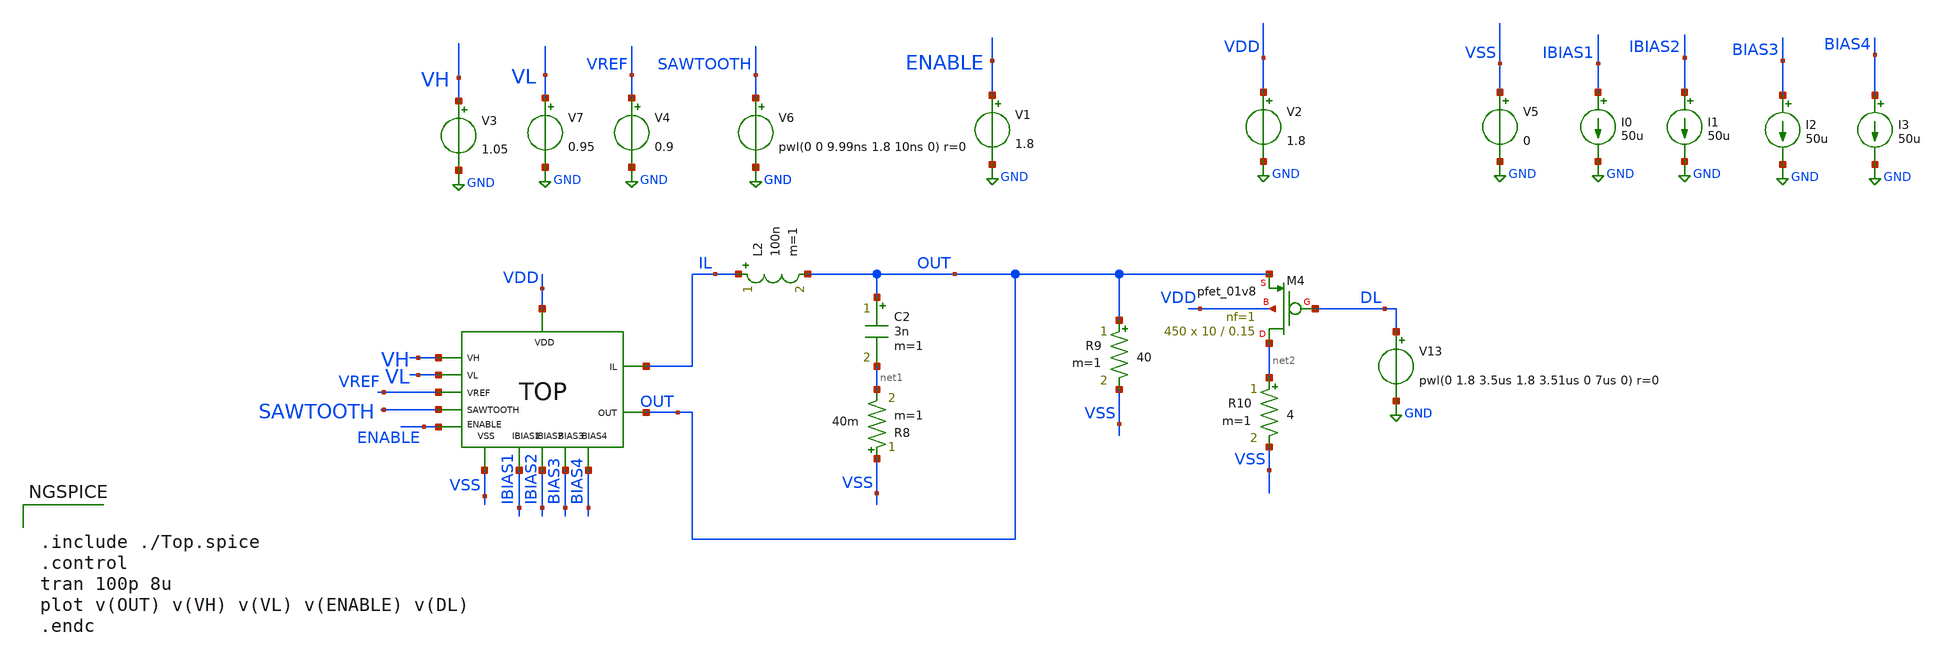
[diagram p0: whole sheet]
** sch_path: xschem/DC_DC_Converter_xschem/DC_DC_Converter/TOP_LEVEL/Top_Final/PEX_TOP/Top_PEX_TB.sch
**.subckt Top_PEX_TB
I0 IBIAS1 GND 50u
V2 VDD GND 1.8
V5 VSS GND 0
V4 VREF GND 0.9
I1 IBIAS2 GND 50u
V6 SAWTOOTH GND pwl(0 0 9.99ns 1.8 10ns 0) r=0
V3 VH GND 1.05
V7 VL GND 0.95
I2 BIAS3 GND 50u
I3 BIAS4 GND 50u
L2 IL OUT 100n m=1
C2 OUT net1 3n m=1
R8 VSS net1 40m m=1
XM4 net2 DL OUT VDD sky130_fd_pr__pfet_01v8 L=0.15 W=10 nf=1 ad='int((nf+1)/2) * W/nf * 0.29' as='int((nf+2)/2) * W/nf * 0.29'
+ pd='2*int((nf+1)/2) * (W/nf + 0.29)' ps='2*int((nf+2)/2) * (W/nf + 0.29)' nrd='0.29 / W' nrs='0.29 / W'
+ sa=0 sb=0 sd=0 mult=450 m=450
V13 DL GND pwl(0 1.8 3.5us 1.8 3.51us 0 7us 0) r=0
R9 OUT VSS 40 m=1
R10 net2 VSS 4 m=1
XTopZ1 VDD VSS VREF IL VH IBIAS1 VL IBIAS2 ENABLE BIAS3 OUT BIAS4 SAWTOOTH Top_PEX
V1 ENABLE GND 1.8
**** begin user architecture code


.include ./Top.spice
.control
tran 100p 8u
plot v(OUT) v(VH) v(VL) v(ENABLE) v(DL)
.endc


** manual skywater pdks install (with patches applied)
* .lib $::SKYWATER_MODELS/models/sky130.lib.spice tt

** opencircuitdesign pdks install
.lib $::SKYWATER_MODELS/sky130.lib.spice tt
.include $::SKYWATER_STDCELLS/sky130_fd_sc_hd.spice

**** end user architecture code
**.ends
.GLOBAL GND
.end
